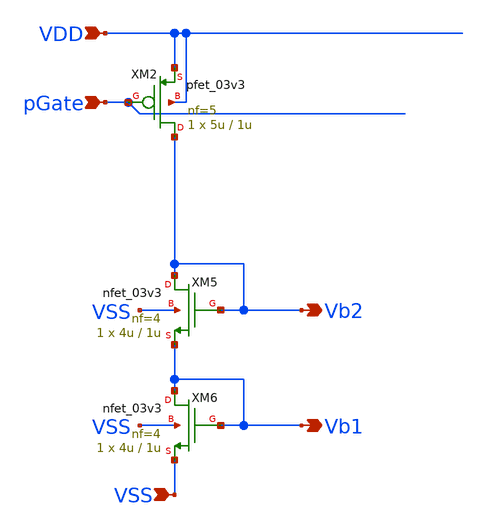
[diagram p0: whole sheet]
** sch_path: DAC/xschem/dac_local_current_mirror.sch
**.subckt dac_local_current_mirror VSS Vb2 Vb1 VDD pGate
*.ipin VSS
*.opin Vb2
*.opin Vb1
*.ipin VDD
*.ipin pGate
XM2 Vb2 pGate VDD VDD pfet_03v3 L=1u W=5u nf=5 ad='int((nf+1)/2) * W/nf * 0.18u' as='int((nf+2)/2) * W/nf * 0.18u'
+ pd='2*int((nf+1)/2) * (W/nf + 0.18u)' ps='2*int((nf+2)/2) * (W/nf + 0.18u)' nrd='0.18u / W' nrs='0.18u / W'
+ sa=0 sb=0 sd=0 m=1
XM5 Vb2 Vb2 Vb1 VSS nfet_03v3 L=1u W=4u nf=4 ad='int((nf+1)/2) * W/nf * 0.18u' as='int((nf+2)/2) * W/nf * 0.18u'
+ pd='2*int((nf+1)/2) * (W/nf + 0.18u)' ps='2*int((nf+2)/2) * (W/nf + 0.18u)' nrd='0.18u / W' nrs='0.18u / W'
+ sa=0 sb=0 sd=0 m=1
XM6 Vb1 Vb1 VSS VSS nfet_03v3 L=1u W=4u nf=4 ad='int((nf+1)/2) * W/nf * 0.18u' as='int((nf+2)/2) * W/nf * 0.18u'
+ pd='2*int((nf+1)/2) * (W/nf + 0.18u)' ps='2*int((nf+2)/2) * (W/nf + 0.18u)' nrd='0.18u / W' nrs='0.18u / W'
+ sa=0 sb=0 sd=0 m=1
**.ends
.end
